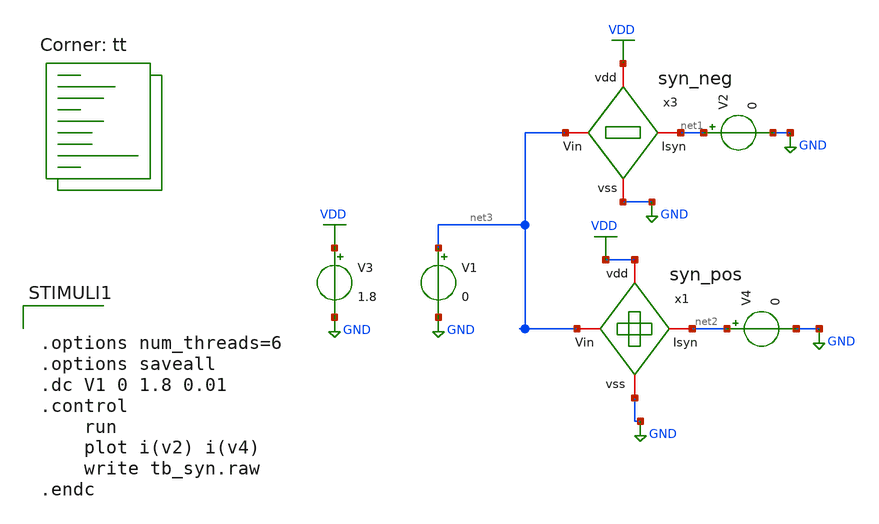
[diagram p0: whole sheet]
** sch_path: Neuron/ultralif/tb_syn.sch
**.subckt tb_syn
V1 net3 GND 0
V2 net1 GND 0
V3 VDD GND 1.8
V4 net2 GND 0
x3 VDD net3 net1 GND syn_neg
x1 VDD net3 net2 GND syn_pos
**** begin user architecture code
.lib $::SKYWATER_MODELS/sky130.lib.spice tt
**** end user architecture code
**.ends

* expanding   symbol:  syn_neg.sym # of pins=4
** sym_path: Neuron/ultralif/syn_neg.sym
** sch_path: Neuron/ultralif/syn_neg.sch
.subckt syn_neg vdd Vin Isyn vss
*.iopin Vin
*.iopin Isyn
*.iopin vdd
*.iopin vss
XM10 Isyn Vin vx vdd sky130_fd_pr__pfet_01v8 L=35 W=0.5 nf=1 ad='int((nf+1)/2) * W/nf * 0.29' as='int((nf+2)/2) * W/nf * 0.29'
+ pd='2*int((nf+1)/2) * (W/nf + 0.29)' ps='2*int((nf+2)/2) * (W/nf + 0.29)' nrd='0.29 / W' nrs='0.29 / W'
+ sa=0 sb=0 sd=0 mult=1 m=1
XM1 vx Vin vdd vdd sky130_fd_pr__pfet_01v8 L=35 W=0.5 nf=1 ad='int((nf+1)/2) * W/nf * 0.29' as='int((nf+2)/2) * W/nf * 0.29'
+ pd='2*int((nf+1)/2) * (W/nf + 0.29)' ps='2*int((nf+2)/2) * (W/nf + 0.29)' nrd='0.29 / W' nrs='0.29 / W'
+ sa=0 sb=0 sd=0 mult=1 m=1
XM2 Isyn net1 vdd vdd sky130_fd_pr__pfet_01v8 L=1 W=0.5 nf=1 ad='int((nf+1)/2) * W/nf * 0.29' as='int((nf+2)/2) * W/nf * 0.29'
+ pd='2*int((nf+1)/2) * (W/nf + 0.29)' ps='2*int((nf+2)/2) * (W/nf + 0.29)' nrd='0.29 / W' nrs='0.29 / W'
+ sa=0 sb=0 sd=0 mult=1 m=1
XR1 net1 vdd sky130_fd_pr__res_generic_po W=1.15 L=1 m=1
XR2 vss net1 sky130_fd_pr__res_generic_po W=1 L=1 m=1
.ends


* expanding   symbol:  syn_pos.sym # of pins=4
** sym_path: Neuron/ultralif/syn_pos.sym
** sch_path: Neuron/ultralif/syn_pos.sch
.subckt syn_pos vdd Vin Isyn vss
*.iopin Vin
*.iopin vdd
*.iopin vss
*.iopin Isyn
XM9 Isyn vx vdd vdd sky130_fd_pr__pfet_01v8 L=1 W=0.5 nf=1 ad='int((nf+1)/2) * W/nf * 0.29' as='int((nf+2)/2) * W/nf * 0.29'
+ pd='2*int((nf+1)/2) * (W/nf + 0.29)' ps='2*int((nf+2)/2) * (W/nf + 0.29)' nrd='0.29 / W' nrs='0.29 / W'
+ sa=0 sb=0 sd=0 mult=1 m=1
XM10 vx vx vdd vdd sky130_fd_pr__pfet_01v8 L=0.15 W=0.5 nf=1 ad='int((nf+1)/2) * W/nf * 0.29' as='int((nf+2)/2) * W/nf * 0.29'
+ pd='2*int((nf+1)/2) * (W/nf + 0.29)' ps='2*int((nf+2)/2) * (W/nf + 0.29)' nrd='0.29 / W' nrs='0.29 / W'
+ sa=0 sb=0 sd=0 mult=5 m=5
XM12 vx Vin vss vss sky130_fd_pr__nfet_01v8 L=1 W=0.4 nf=1 ad='int((1 + 1)/2) * 0.4 / 1 * 0.29' as='int((1 + 2)/2) * 0.4 / 1 * 0.29'
+ pd='2*int((1 + 1)/2) * (0.4 / 1 + 0.29)' ps='2*int((1 + 2)/2) * (0.4 / 1 + 0.29)' nrd='0.29 / 0.4 ' nrs='0.29 / 0.4 '
+ sa=0 sb=0 sd=0 mult=1 m=1
.ends

.GLOBAL GND
.GLOBAL VDD
**** begin user architecture code


.options num_threads=6
.options saveall
.dc V1 0 1.8 0.01
.control
	run
	plot i(v2) i(v4)
	write tb_syn.raw
.endc


**** end user architecture code
.end
